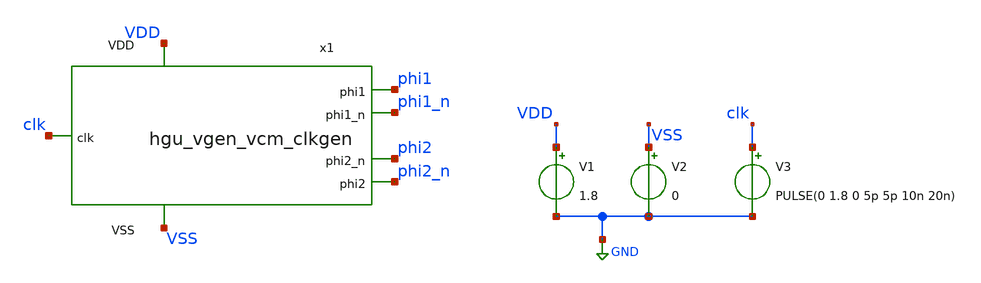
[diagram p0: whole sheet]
** sch_path: tb/tb_hgu_vgen_vcm.sch
**.subckt tb_hgu_vgen_vcm
x1 VDD VSS phi1 clk phi1_n phi2 phi2_n hgu_vgen_vcm_clkgen
V1 VDD GND 1.8
V2 VSS GND 0
V3 clk GND PULSE(0 1.8 0 5p 5p 10n 20n)
**** begin user architecture code



.lib /foss/pdks/sky130A/libs.tech/ngspice/sky130.lib.spice tt
.include /foss/pdks/sky130A/libs.ref/sky130_fd_sc_hd/spice/sky130_fd_sc_hd.spice

.tran 1ns 200ns
.control
    run
    plot V(phi1)+2 V(phi1_n)+2  V(phi2)+4  V(phi2_n)+4 V(clk)
.endc
.save all



**** end user architecture code
**.ends
.GLOBAL GND
.end
